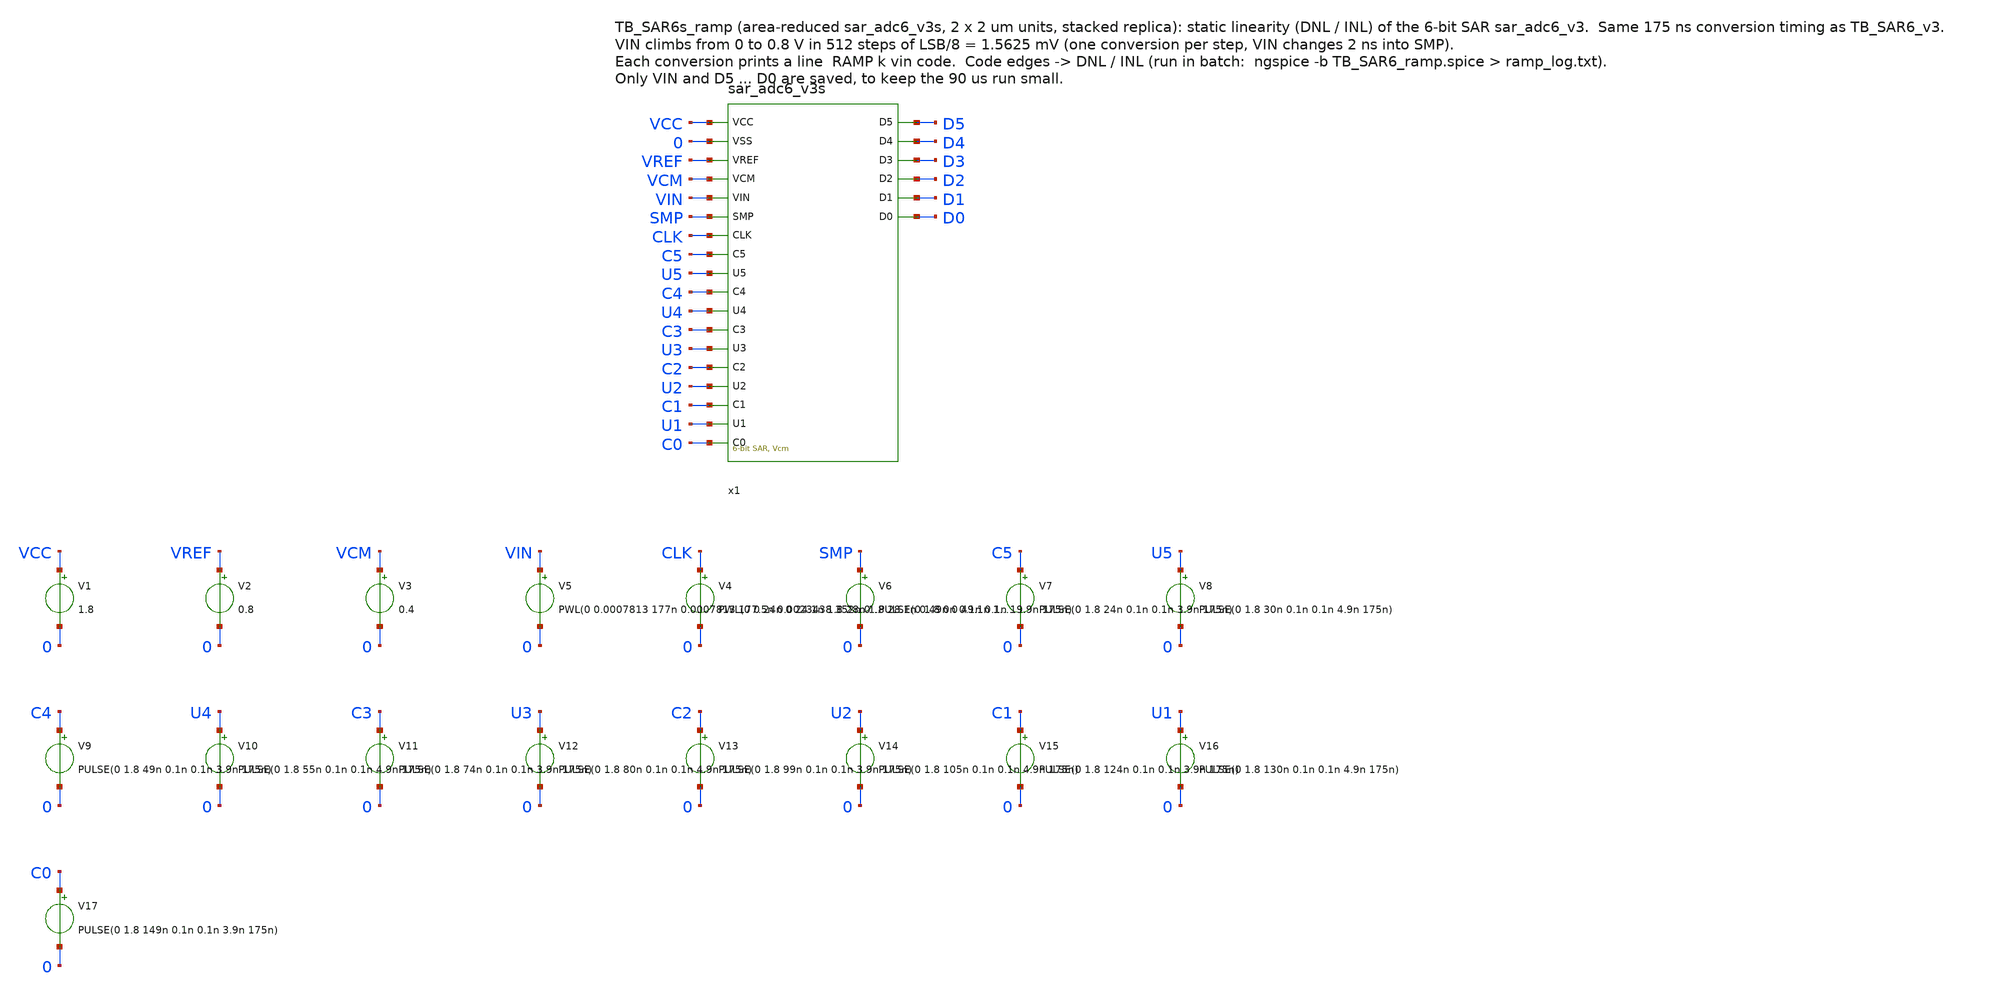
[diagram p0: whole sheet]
** sch_path: SAR_improved/TB_SAR6s_ramp.sch
**.subckt TB_SAR6s_ramp
x1 VCC 0 VREF VCM VIN SMP CLK C5 U5 C4 U4 C3 U3 C2 U2 C1 U1 C0 D5 D4 D3 D2 D1 D0 sar_adc6_v3s
V1 VCC 0 1.8
V2 VREF 0 0.8
V3 VCM 0 0.4
V5 VIN 0 PWL(0 0.0007813 177n 0.0007813 177.5n 0.0023438 352n 0.0023438 352.5n 0.0039062 527n
+ 0.0039062 527.5n 0.0054688 702n 0.0054688 702.5n 0.0070313 877n 0.0070313 877.5n 0.0085938 1052n 0.0085938
+ 1052.5n 0.0101563 1227n 0.0101563 1227.5n 0.0117188 1402n 0.0117188 1402.5n 0.0132813 1577n 0.0132813
+ 1577.5n 0.0148438 1752n 0.0148438 1752.5n 0.0164063 1927n 0.0164063 1927.5n 0.0179688 2102n 0.0179688
+ 2102.5n 0.0195312 2277n 0.0195312 2277.5n 0.0210938 2452n 0.0210938 2452.5n 0.0226563 2627n 0.0226563
+ 2627.5n 0.0242188 2802n 0.0242188 2802.5n 0.0257813 2977n 0.0257813 2977.5n 0.0273438 3152n 0.0273438
+ 3152.5n 0.0289063 3327n 0.0289063 3327.5n 0.0304688 3502n 0.0304688 3502.5n 0.0320313 3677n 0.0320313
+ 3677.5n 0.0335937 3852n 0.0335937 3852.5n 0.0351562 4027n 0.0351562 4027.5n 0.0367188 4202n 0.0367188
+ 4202.5n 0.0382813 4377n 0.0382813 4377.5n 0.0398438 4552n 0.0398438 4552.5n 0.0414063 4727n 0.0414063
+ 4727.5n 0.0429688 4902n 0.0429688 4902.5n 0.0445313 5077n 0.0445313 5077.5n 0.0460938 5252n 0.0460938
+ 5252.5n 0.0476563 5427n 0.0476563 5427.5n 0.0492188 5602n 0.0492188 5602.5n 0.0507812 5777n 0.0507812
+ 5777.5n 0.0523438 5952n 0.0523438 5952.5n 0.0539063 6127n 0.0539063 6127.5n 0.0554688 6302n 0.0554688
+ 6302.5n 0.0570313 6477n 0.0570313 6477.5n 0.0585938 6652n 0.0585938 6652.5n 0.0601563 6827n 0.0601563
+ 6827.5n 0.0617188 7002n 0.0617188 7002.5n 0.0632812 7177n 0.0632812 7177.5n 0.0648438 7352n 0.0648438
+ 7352.5n 0.0664062 7527n 0.0664062 7527.5n 0.0679688 7702n 0.0679688 7702.5n 0.0695313 7877n 0.0695313
+ 7877.5n 0.0710937 8052n 0.0710937 8052.5n 0.0726563 8227n 0.0726563 8227.5n 0.0742188 8402n 0.0742188
+ 8402.5n 0.0757813 8577n 0.0757813 8577.5n 0.0773438 8752n 0.0773438 8752.5n 0.0789063 8927n 0.0789063
+ 8927.5n 0.0804688 9102n 0.0804688 9102.5n 0.0820312 9277n 0.0820312 9277.5n 0.0835938 9452n 0.0835938
+ 9452.5n 0.0851563 9627n 0.0851563 9627.5n 0.0867188 9802n 0.0867188 9802.5n 0.0882813 9977n 0.0882813
+ 9977.5n 0.0898438 10152n 0.0898438 10152.5n 0.0914063 10327n 0.0914063 10327.5n 0.0929688 10502n 0.0929688
+ 10502.5n 0.0945313 10677n 0.0945313 10677.5n 0.0960938 10852n 0.0960938 10852.5n 0.0976562 11027n 0.0976562
+ 11027.5n 0.0992188 11202n 0.0992188 11202.5n 0.1007813 11377n 0.1007813 11377.5n 0.1023438 11552n 0.1023438
+ 11552.5n 0.1039063 11727n 0.1039063 11727.5n 0.1054688 11902n 0.1054688 11902.5n 0.1070313 12077n 0.1070313
+ 12077.5n 0.1085938 12252n 0.1085938 12252.5n 0.1101563 12427n 0.1101563 12427.5n 0.1117188 12602n 0.1117188
+ 12602.5n 0.1132812 12777n 0.1132812 12777.5n 0.1148438 12952n 0.1148438 12952.5n 0.1164063 13127n 0.1164063
+ 13127.5n 0.1179688 13302n 0.1179688 13302.5n 0.1195313 13477n 0.1195313 13477.5n 0.1210938 13652n 0.1210938
+ 13652.5n 0.1226563 13827n 0.1226563 13827.5n 0.1242188 14002n 0.1242188 14002.5n 0.1257813 14177n 0.1257813
+ 14177.5n 0.1273438 14352n 0.1273438 14352.5n 0.1289062 14527n 0.1289062 14527.5n 0.1304687 14702n 0.1304687
+ 14702.5n 0.1320313 14877n 0.1320313 14877.5n 0.1335938 15052n 0.1335938 15052.5n 0.1351563 15227n 0.1351563
+ 15227.5n 0.1367188 15402n 0.1367188 15402.5n 0.1382812 15577n 0.1382812 15577.5n 0.1398438 15752n 0.1398438
+ 15752.5n 0.1414063 15927n 0.1414063 15927.5n 0.1429688 16102n 0.1429688 16102.5n 0.1445312 16277n 0.1445312
+ 16277.5n 0.1460937 16452n 0.1460937 16452.5n 0.1476563 16627n 0.1476563 16627.5n 0.1492188 16802n 0.1492188
+ 16802.5n 0.1507813 16977n 0.1507813 16977.5n 0.1523438 17152n 0.1523438 17152.5n 0.1539063 17327n 0.1539063
+ 17327.5n 0.1554688 17502n 0.1554688 17502.5n 0.1570313 17677n 0.1570313 17677.5n 0.1585938 17852n 0.1585938
+ 17852.5n 0.1601562 18027n 0.1601562 18027.5n 0.1617188 18202n 0.1617188 18202.5n 0.1632813 18377n 0.1632813
+ 18377.5n 0.1648438 18552n 0.1648438 18552.5n 0.1664063 18727n 0.1664063 18727.5n 0.1679688 18902n 0.1679688
+ 18902.5n 0.1695313 19077n 0.1695313 19077.5n 0.1710938 19252n 0.1710938 19252.5n 0.1726563 19427n 0.1726563
+ 19427.5n 0.1742188 19602n 0.1742188 19602.5n 0.1757812 19777n 0.1757812 19777.5n 0.1773438 19952n 0.1773438
+ 19952.5n 0.1789063 20127n 0.1789063 20127.5n 0.1804688 20302n 0.1804688 20302.5n 0.1820313 20477n 0.1820313
+ 20477.5n 0.1835938 20652n 0.1835938 20652.5n 0.1851563 20827n 0.1851563 20827.5n 0.1867188 21002n 0.1867188
+ 21002.5n 0.1882813 21177n 0.1882813 21177.5n 0.1898438 21352n 0.1898438 21352.5n 0.1914062 21527n 0.1914062
+ 21527.5n 0.1929688 21702n 0.1929688 21702.5n 0.1945313 21877n 0.1945313 21877.5n 0.1960938 22052n 0.1960938
+ 22052.5n 0.1976563 22227n 0.1976563 22227.5n 0.1992188 22402n 0.1992188 22402.5n 0.2007813 22577n 0.2007813
+ 22577.5n 0.2023438 22752n 0.2023438 22752.5n 0.2039063 22927n 0.2039063 22927.5n 0.2054688 23102n 0.2054688
+ 23102.5n 0.2070312 23277n 0.2070312 23277.5n 0.2085938 23452n 0.2085938 23452.5n 0.2101563 23627n 0.2101563
+ 23627.5n 0.2117188 23802n 0.2117188 23802.5n 0.2132813 23977n 0.2132813 23977.5n 0.2148438 24152n 0.2148438
+ 24152.5n 0.2164063 24327n 0.2164063 24327.5n 0.2179688 24502n 0.2179688 24502.5n 0.2195313 24677n 0.2195313
+ 24677.5n 0.2210938 24852n 0.2210938 24852.5n 0.2226562 25027n 0.2226562 25027.5n 0.2242188 25202n 0.2242188
+ 25202.5n 0.2257813 25377n 0.2257813 25377.5n 0.2273438 25552n 0.2273438 25552.5n 0.2289063 25727n 0.2289063
+ 25727.5n 0.2304688 25902n 0.2304688 25902.5n 0.2320313 26077n 0.2320313 26077.5n 0.2335938 26252n 0.2335938
+ 26252.5n 0.2351563 26427n 0.2351563 26427.5n 0.2367188 26602n 0.2367188 26602.5n 0.2382812 26777n 0.2382812
+ 26777.5n 0.2398438 26952n 0.2398438 26952.5n 0.2414063 27127n 0.2414063 27127.5n 0.2429688 27302n 0.2429688
+ 27302.5n 0.2445313 27477n 0.2445313 27477.5n 0.2460938 27652n 0.2460938 27652.5n 0.2476563 27827n 0.2476563
+ 27827.5n 0.2492188 28002n 0.2492188 28002.5n 0.2507813 28177n 0.2507813 28177.5n 0.2523438 28352n 0.2523438
+ 28352.5n 0.2539062 28527n 0.2539062 28527.5n 0.2554688 28702n 0.2554688 28702.5n 0.2570312 28877n 0.2570312
+ 28877.5n 0.2585938 29052n 0.2585938 29052.5n 0.2601563 29227n 0.2601563 29227.5n 0.2617188 29402n 0.2617188
+ 29402.5n 0.2632813 29577n 0.2632813 29577.5n 0.2648437 29752n 0.2648437 29752.5n 0.2664063 29927n 0.2664063
+ 29927.5n 0.2679688 30102n 0.2679688 30102.5n 0.2695312 30277n 0.2695312 30277.5n 0.2710938 30452n 0.2710938
+ 30452.5n 0.2726562 30627n 0.2726562 30627.5n 0.2742188 30802n 0.2742188 30802.5n 0.2757813 30977n 0.2757813
+ 30977.5n 0.2773438 31152n 0.2773438 31152.5n 0.2789063 31327n 0.2789063 31327.5n 0.2804687 31502n 0.2804687
+ 31502.5n 0.2820313 31677n 0.2820313 31677.5n 0.2835938 31852n 0.2835938 31852.5n 0.2851562 32027n 0.2851562
+ 32027.5n 0.2867188 32202n 0.2867188 32202.5n 0.2882812 32377n 0.2882812 32377.5n 0.2898438 32552n 0.2898438
+ 32552.5n 0.2914063 32727n 0.2914063 32727.5n 0.2929688 32902n 0.2929688 32902.5n 0.2945313 33077n 0.2945313
+ 33077.5n 0.2960937 33252n 0.2960937 33252.5n 0.2976563 33427n 0.2976563 33427.5n 0.2992188 33602n 0.2992188
+ 33602.5n 0.3007812 33777n 0.3007812 33777.5n 0.3023438 33952n 0.3023438 33952.5n 0.3039063 34127n 0.3039063
+ 34127.5n 0.3054688 34302n 0.3054688 34302.5n 0.3070313 34477n 0.3070313 34477.5n 0.3085938 34652n 0.3085938
+ 34652.5n 0.3101563 34827n 0.3101563 34827.5n 0.3117188 35002n 0.3117188 35002.5n 0.3132813 35177n 0.3132813
+ 35177.5n 0.3148438 35352n 0.3148438 35352.5n 0.3164062 35527n 0.3164062 35527.5n 0.3179688 35702n 0.3179688
+ 35702.5n 0.3195313 35877n 0.3195313 35877.5n 0.3210938 36052n 0.3210938 36052.5n 0.3226563 36227n 0.3226563
+ 36227.5n 0.3242188 36402n 0.3242188 36402.5n 0.3257813 36577n 0.3257813 36577.5n 0.3273438 36752n 0.3273438
+ 36752.5n 0.3289063 36927n 0.3289063 36927.5n 0.3304688 37102n 0.3304688 37102.5n 0.3320312 37277n 0.3320312
+ 37277.5n 0.3335938 37452n 0.3335938 37452.5n 0.3351563 37627n 0.3351563 37627.5n 0.3367188 37802n 0.3367188
+ 37802.5n 0.3382813 37977n 0.3382813 37977.5n 0.3398438 38152n 0.3398438 38152.5n 0.3414063 38327n 0.3414063
+ 38327.5n 0.3429688 38502n 0.3429688 38502.5n 0.3445313 38677n 0.3445313 38677.5n 0.3460938 38852n 0.3460938
+ 38852.5n 0.3476562 39027n 0.3476562 39027.5n 0.3492188 39202n 0.3492188 39202.5n 0.3507813 39377n 0.3507813
+ 39377.5n 0.3523438 39552n 0.3523438 39552.5n 0.3539063 39727n 0.3539063 39727.5n 0.3554688 39902n 0.3554688
+ 39902.5n 0.3570313 40077n 0.3570313 40077.5n 0.3585938 40252n 0.3585938 40252.5n 0.3601563 40427n 0.3601563
+ 40427.5n 0.3617188 40602n 0.3617188 40602.5n 0.3632812 40777n 0.3632812 40777.5n 0.3648438 40952n 0.3648438
+ 40952.5n 0.3664063 41127n 0.3664063 41127.5n 0.3679688 41302n 0.3679688 41302.5n 0.3695313 41477n 0.3695313
+ 41477.5n 0.3710938 41652n 0.3710938 41652.5n 0.3726563 41827n 0.3726563 41827.5n 0.3742188 42002n 0.3742188
+ 42002.5n 0.3757813 42177n 0.3757813 42177.5n 0.3773438 42352n 0.3773438 42352.5n 0.3789062 42527n 0.3789062
+ 42527.5n 0.3804688 42702n 0.3804688 42702.5n 0.3820313 42877n 0.3820313 42877.5n 0.3835938 43052n 0.3835938
+ 43052.5n 0.3851563 43227n 0.3851563 43227.5n 0.3867188 43402n 0.3867188 43402.5n 0.3882813 43577n 0.3882813
+ 43577.5n 0.3898438 43752n 0.3898438 43752.5n 0.3914063 43927n 0.3914063 43927.5n 0.3929688 44102n 0.3929688
+ 44102.5n 0.3945312 44277n 0.3945312 44277.5n 0.3960938 44452n 0.3960938 44452.5n 0.3976563 44627n 0.3976563
+ 44627.5n 0.3992188 44802n 0.3992188 44802.5n 0.4007813 44977n 0.4007813 44977.5n 0.4023438 45152n 0.4023438
+ 45152.5n 0.4039063 45327n 0.4039063 45327.5n 0.4054688 45502n 0.4054688 45502.5n 0.4070313 45677n 0.4070313
+ 45677.5n 0.4085938 45852n 0.4085938 45852.5n 0.4101562 46027n 0.4101562 46027.5n 0.4117188 46202n 0.4117188
+ 46202.5n 0.4132813 46377n 0.4132813 46377.5n 0.4148438 46552n 0.4148438 46552.5n 0.4164063 46727n 0.4164063
+ 46727.5n 0.4179688 46902n 0.4179688 46902.5n 0.4195313 47077n 0.4195313 47077.5n 0.4210938 47252n 0.4210938
+ 47252.5n 0.4226563 47427n 0.4226563 47427.5n 0.4242188 47602n 0.4242188 47602.5n 0.4257812 47777n 0.4257812
+ 47777.5n 0.4273438 47952n 0.4273438 47952.5n 0.4289063 48127n 0.4289063 48127.5n 0.4304688 48302n 0.4304688
+ 48302.5n 0.4320313 48477n 0.4320313 48477.5n 0.4335938 48652n 0.4335938 48652.5n 0.4351563 48827n 0.4351563
+ 48827.5n 0.4367188 49002n 0.4367188 49002.5n 0.4382813 49177n 0.4382813 49177.5n 0.4398438 49352n 0.4398438
+ 49352.5n 0.4414062 49527n 0.4414062 49527.5n 0.4429688 49702n 0.4429688 49702.5n 0.4445313 49877n 0.4445313
+ 49877.5n 0.4460938 50052n 0.4460938 50052.5n 0.4476563 50227n 0.4476563 50227.5n 0.4492188 50402n 0.4492188
+ 50402.5n 0.4507813 50577n 0.4507813 50577.5n 0.4523438 50752n 0.4523438 50752.5n 0.4539063 50927n 0.4539063
+ 50927.5n 0.4554688 51102n 0.4554688 51102.5n 0.4570312 51277n 0.4570312 51277.5n 0.4585938 51452n 0.4585938
+ 51452.5n 0.4601563 51627n 0.4601563 51627.5n 0.4617188 51802n 0.4617188 51802.5n 0.4632813 51977n 0.4632813
+ 51977.5n 0.4648438 52152n 0.4648438 52152.5n 0.4664063 52327n 0.4664063 52327.5n 0.4679688 52502n 0.4679688
+ 52502.5n 0.4695313 52677n 0.4695313 52677.5n 0.4710938 52852n 0.4710938 52852.5n 0.4726562 53027n 0.4726562
+ 53027.5n 0.4742188 53202n 0.4742188 53202.5n 0.4757813 53377n 0.4757813 53377.5n 0.4773438 53552n 0.4773438
+ 53552.5n 0.4789063 53727n 0.4789063 53727.5n 0.4804688 53902n 0.4804688 53902.5n 0.4820313 54077n 0.4820313
+ 54077.5n 0.4835938 54252n 0.4835938 54252.5n 0.4851563 54427n 0.4851563 54427.5n 0.4867188 54602n 0.4867188
+ 54602.5n 0.4882812 54777n 0.4882812 54777.5n 0.4898438 54952n 0.4898438 54952.5n 0.4914063 55127n 0.4914063
+ 55127.5n 0.4929688 55302n 0.4929688 55302.5n 0.4945313 55477n 0.4945313 55477.5n 0.4960938 55652n 0.4960938
+ 55652.5n 0.4976563 55827n 0.4976563 55827.5n 0.4992188 56002n 0.4992188 56002.5n 0.5007813 56177n 0.5007813
+ 56177.5n 0.5023437 56352n 0.5023437 56352.5n 0.5039062 56527n 0.5039062 56527.5n 0.5054688 56702n 0.5054688
+ 56702.5n 0.5070313 56877n 0.5070313 56877.5n 0.5085938 57052n 0.5085938 57052.5n 0.5101562 57227n 0.5101562
+ 57227.5n 0.5117188 57402n 0.5117188 57402.5n 0.5132813 57577n 0.5132813 57577.5n 0.5148438 57752n 0.5148438
+ 57752.5n 0.5164063 57927n 0.5164063 57927.5n 0.5179687 58102n 0.5179687 58102.5n 0.5195312 58277n 0.5195312
+ 58277.5n 0.5210938 58452n 0.5210938 58452.5n 0.5226563 58627n 0.5226563 58627.5n 0.5242188 58802n 0.5242188
+ 58802.5n 0.5257812 58977n 0.5257812 58977.5n 0.5273438 59152n 0.5273438 59152.5n 0.5289063 59327n 0.5289063
+ 59327.5n 0.5304688 59502n 0.5304688 59502.5n 0.5320313 59677n 0.5320313 59677.5n 0.5335937 59852n 0.5335937
+ 59852.5n 0.5351562 60027n 0.5351562 60027.5n 0.5367188 60202n 0.5367188 60202.5n 0.5382813 60377n 0.5382813
+ 60377.5n 0.5398438 60552n 0.5398438 60552.5n 0.5414062 60727n 0.5414062 60727.5n 0.5429688 60902n 0.5429688
+ 60902.5n 0.5445313 61077n 0.5445313 61077.5n 0.5460938 61252n 0.5460938 61252.5n 0.5476563 61427n 0.5476563
+ 61427.5n 0.5492187 61602n 0.5492187 61602.5n 0.5507812 61777n 0.5507812 61777.5n 0.5523438 61952n 0.5523438
+ 61952.5n 0.5539063 62127n 0.5539063 62127.5n 0.5554688 62302n 0.5554688 62302.5n 0.5570312 62477n 0.5570312
+ 62477.5n 0.5585938 62652n 0.5585938 62652.5n 0.5601563 62827n 0.5601563 62827.5n 0.5617188 63002n 0.5617188
+ 63002.5n 0.5632813 63177n 0.5632813 63177.5n 0.5648437 63352n 0.5648437 63352.5n 0.5664062 63527n 0.5664062
+ 63527.5n 0.5679688 63702n 0.5679688 63702.5n 0.5695313 63877n 0.5695313 63877.5n 0.5710938 64052n 0.5710938
+ 64052.5n 0.5726562 64227n 0.5726562 64227.5n 0.5742188 64402n 0.5742188 64402.5n 0.5757813 64577n 0.5757813
+ 64577.5n 0.5773438 64752n 0.5773438 64752.5n 0.5789063 64927n 0.5789063 64927.5n 0.5804687 65102n 0.5804687
+ 65102.5n 0.5820312 65277n 0.5820312 65277.5n 0.5835938 65452n 0.5835938 65452.5n 0.5851563 65627n 0.5851563
+ 65627.5n 0.5867188 65802n 0.5867188 65802.5n 0.5882812 65977n 0.5882812 65977.5n 0.5898438 66152n 0.5898438
+ 66152.5n 0.5914063 66327n 0.5914063 66327.5n 0.5929688 66502n 0.5929688 66502.5n 0.5945313 66677n 0.5945313
+ 66677.5n 0.5960937 66852n 0.5960937 66852.5n 0.5976562 67027n 0.5976562 67027.5n 0.5992188 67202n 0.5992188
+ 67202.5n 0.6007813 67377n 0.6007813 67377.5n 0.6023438 67552n 0.6023438 67552.5n 0.6039063 67727n 0.6039063
+ 67727.5n 0.6054688 67902n 0.6054688 67902.5n 0.6070313 68077n 0.6070313 68077.5n 0.6085938 68252n 0.6085938
+ 68252.5n 0.6101563 68427n 0.6101563 68427.5n 0.6117188 68602n 0.6117188 68602.5n 0.6132812 68777n 0.6132812
+ 68777.5n 0.6148438 68952n 0.6148438 68952.5n 0.6164063 69127n 0.6164063 69127.5n 0.6179688 69302n 0.6179688
+ 69302.5n 0.6195313 69477n 0.6195313 69477.5n 0.6210938 69652n 0.6210938 69652.5n 0.6226563 69827n 0.6226563
+ 69827.5n 0.6242188 70002n 0.6242188 70002.5n 0.6257813 70177n 0.6257813 70177.5n 0.6273438 70352n 0.6273438
+ 70352.5n 0.6289062 70527n 0.6289062 70527.5n 0.6304688 70702n 0.6304688 70702.5n 0.6320313 70877n 0.6320313
+ 70877.5n 0.6335938 71052n 0.6335938 71052.5n 0.6351563 71227n 0.6351563 71227.5n 0.6367188 71402n 0.6367188
+ 71402.5n 0.6382813 71577n 0.6382813 71577.5n 0.6398438 71752n 0.6398438 71752.5n 0.6414063 71927n 0.6414063
+ 71927.5n 0.6429688 72102n 0.6429688 72102.5n 0.6445312 72277n 0.6445312 72277.5n 0.6460938 72452n 0.6460938
+ 72452.5n 0.6476563 72627n 0.6476563 72627.5n 0.6492188 72802n 0.6492188 72802.5n 0.6507813 72977n 0.6507813
+ 72977.5n 0.6523438 73152n 0.6523438 73152.5n 0.6539063 73327n 0.6539063 73327.5n 0.6554688 73502n 0.6554688
+ 73502.5n 0.6570313 73677n 0.6570313 73677.5n 0.6585938 73852n 0.6585938 73852.5n 0.6601562 74027n 0.6601562
+ 74027.5n 0.6617188 74202n 0.6617188 74202.5n 0.6632813 74377n 0.6632813 74377.5n 0.6648438 74552n 0.6648438
+ 74552.5n 0.6664063 74727n 0.6664063 74727.5n 0.6679688 74902n 0.6679688 74902.5n 0.6695313 75077n 0.6695313
+ 75077.5n 0.6710938 75252n 0.6710938 75252.5n 0.6726563 75427n 0.6726563 75427.5n 0.6742188 75602n 0.6742188
+ 75602.5n 0.6757812 75777n 0.6757812 75777.5n 0.6773438 75952n 0.6773438 75952.5n 0.6789063 76127n 0.6789063
+ 76127.5n 0.6804688 76302n 0.6804688 76302.5n 0.6820313 76477n 0.6820313 76477.5n 0.6835938 76652n 0.6835938
+ 76652.5n 0.6851563 76827n 0.6851563 76827.5n 0.6867188 77002n 0.6867188 77002.5n 0.6882813 77177n 0.6882813
+ 77177.5n 0.6898438 77352n 0.6898438 77352.5n 0.6914062 77527n 0.6914062 77527.5n 0.6929688 77702n 0.6929688
+ 77702.5n 0.6945313 77877n 0.6945313 77877.5n 0.6960938 78052n 0.6960938 78052.5n 0.6976563 78227n 0.6976563
+ 78227.5n 0.6992188 78402n 0.6992188 78402.5n 0.7007813 78577n 0.7007813 78577.5n 0.7023438 78752n 0.7023438
+ 78752.5n 0.7039063 78927n 0.7039063 78927.5n 0.7054688 79102n 0.7054688 79102.5n 0.7070312 79277n 0.7070312
+ 79277.5n 0.7085938 79452n 0.7085938 79452.5n 0.7101563 79627n 0.7101563 79627.5n 0.7117188 79802n 0.7117188
+ 79802.5n 0.7132813 79977n 0.7132813 79977.5n 0.7148438 80152n 0.7148438 80152.5n 0.7164063 80327n 0.7164063
+ 80327.5n 0.7179688 80502n 0.7179688 80502.5n 0.7195313 80677n 0.7195313 80677.5n 0.7210938 80852n 0.7210938
+ 80852.5n 0.7226562 81027n 0.7226562 81027.5n 0.7242188 81202n 0.7242188 81202.5n 0.7257813 81377n 0.7257813
+ 81377.5n 0.7273438 81552n 0.7273438 81552.5n 0.7289063 81727n 0.7289063 81727.5n 0.7304688 81902n 0.7304688
+ 81902.5n 0.7320313 82077n 0.7320313 82077.5n 0.7335938 82252n 0.7335938 82252.5n 0.7351563 82427n 0.7351563
+ 82427.5n 0.7367188 82602n 0.7367188 82602.5n 0.7382812 82777n 0.7382812 82777.5n 0.7398438 82952n 0.7398438
+ 82952.5n 0.7414063 83127n 0.7414063 83127.5n 0.7429688 83302n 0.7429688 83302.5n 0.7445313 83477n 0.7445313
+ 83477.5n 0.7460938 83652n 0.7460938 83652.5n 0.7476563 83827n 0.7476563 83827.5n 0.7492188 84002n 0.7492188
+ 84002.5n 0.7507813 84177n 0.7507813 84177.5n 0.7523438 84352n 0.7523438 84352.5n 0.7539062 84527n 0.7539062
+ 84527.5n 0.7554688 84702n 0.7554688 84702.5n 0.7570313 84877n 0.7570313 84877.5n 0.7585938 85052n 0.7585938
+ 85052.5n 0.7601563 85227n 0.7601563 85227.5n 0.7617188 85402n 0.7617188 85402.5n 0.7632813 85577n 0.7632813
+ 85577.5n 0.7648438 85752n 0.7648438 85752.5n 0.7664063 85927n 0.7664063 85927.5n 0.7679688 86102n 0.7679688
+ 86102.5n 0.7695312 86277n 0.7695312 86277.5n 0.7710938 86452n 0.7710938 86452.5n 0.7726563 86627n 0.7726563
+ 86627.5n 0.7742188 86802n 0.7742188 86802.5n 0.7757813 86977n 0.7757813 86977.5n 0.7773438 87152n 0.7773438
+ 87152.5n 0.7789063 87327n 0.7789063 87327.5n 0.7804688 87502n 0.7804688 87502.5n 0.7820313 87677n 0.7820313
+ 87677.5n 0.7835938 87852n 0.7835938 87852.5n 0.7851562 88027n 0.7851562 88027.5n 0.7867188 88202n 0.7867188
+ 88202.5n 0.7882813 88377n 0.7882813 88377.5n 0.7898438 88552n 0.7898438 88552.5n 0.7914063 88727n 0.7914063
+ 88727.5n 0.7929688 88902n 0.7929688 88902.5n 0.7945313 89077n 0.7945313 89077.5n 0.7960938 89252n 0.7960938
+ 89252.5n 0.7976563 89427n 0.7976563 89427.5n 0.7992188)
V4 CLK 0 PWL(0 0 24n 0 24.1n 1.8 28n 1.8 28.1n 0 49n 0 49.1n 1.8 53n 1.8 53.1n 0 74n 0 74.1n 1.8 78n
+ 1.8 78.1n 0 99n 0 99.1n 1.8 103n 1.8 103.1n 0 124n 0 124.1n 1.8 128n 1.8 128.1n 0 149n 0 149.1n 1.8
+ 153n 1.8 153.1n 0 175n 0) r=0
V6 SMP 0 PULSE(0 1.8 0n 0.1n 0.1n 19.9n 175n)
V7 C5 0 PULSE(0 1.8 24n 0.1n 0.1n 3.9n 175n)
V8 U5 0 PULSE(0 1.8 30n 0.1n 0.1n 4.9n 175n)
V9 C4 0 PULSE(0 1.8 49n 0.1n 0.1n 3.9n 175n)
V10 U4 0 PULSE(0 1.8 55n 0.1n 0.1n 4.9n 175n)
V11 C3 0 PULSE(0 1.8 74n 0.1n 0.1n 3.9n 175n)
V12 U3 0 PULSE(0 1.8 80n 0.1n 0.1n 4.9n 175n)
V13 C2 0 PULSE(0 1.8 99n 0.1n 0.1n 3.9n 175n)
V14 U2 0 PULSE(0 1.8 105n 0.1n 0.1n 4.9n 175n)
V15 C1 0 PULSE(0 1.8 124n 0.1n 0.1n 3.9n 175n)
V16 U1 0 PULSE(0 1.8 130n 0.1n 0.1n 4.9n 175n)
V17 C0 0 PULSE(0 1.8 149n 0.1n 0.1n 3.9n 175n)
**** begin user architecture code

.lib /home/ttuser/pdk/sky130A/libs.tech/combined/sky130.lib.spice tt
.option method=gear reltol=1e-4
.control
save v(VIN) v(D5) v(D4) v(D3) v(D2) v(D1) v(D0)
tran 0.1n 89600n
let code = 0*v(D0)
let code = code + 32*ceil((v(D5)-0.9)/10)
let code = code + 16*ceil((v(D4)-0.9)/10)
let code = code + 8*ceil((v(D3)-0.9)/10)
let code = code + 4*ceil((v(D2)-0.9)/10)
let code = code + 2*ceil((v(D1)-0.9)/10)
let code = code + 1*ceil((v(D0)-0.9)/10)
let k = 0
while k < 512
  let tr = k*175e-9 + 165e-9
  meas tran ck find code at=$&tr
  meas tran vk find v(VIN) at=$&tr
  echo RAMP $&k $&vk $&ck
  let k = k + 1
end
plot code
.endc

**** end user architecture code
**.ends
.end
